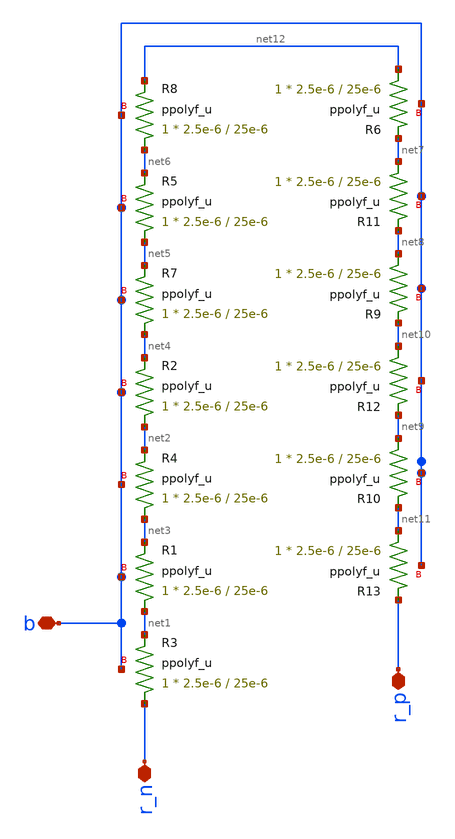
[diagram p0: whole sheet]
** sch_path: designs/libs/core_analog/vref/vref_R2.sch
**.subckt vref_R2 r_p r_n b
*.iopin r_p
*.iopin r_n
*.iopin b
XR1 net1 net3 b ppolyf_u r_width=2.5e-6 r_length=25e-6 m=1
XR2 net2 net4 b ppolyf_u r_width=2.5e-6 r_length=25e-6 m=1
XR3 r_n net1 b ppolyf_u r_width=2.5e-6 r_length=25e-6 m=1
XR4 net3 net2 b ppolyf_u r_width=2.5e-6 r_length=25e-6 m=1
XR5 net5 net6 b ppolyf_u r_width=2.5e-6 r_length=25e-6 m=1
XR7 net4 net5 b ppolyf_u r_width=2.5e-6 r_length=25e-6 m=1
XR8 net6 net12 b ppolyf_u r_width=2.5e-6 r_length=25e-6 m=1
XR6 net12 net7 b ppolyf_u r_width=2.5e-6 r_length=25e-6 m=1
XR9 net8 net10 b ppolyf_u r_width=2.5e-6 r_length=25e-6 m=1
XR10 net9 net11 b ppolyf_u r_width=2.5e-6 r_length=25e-6 m=1
XR11 net7 net8 b ppolyf_u r_width=2.5e-6 r_length=25e-6 m=1
XR12 net10 net9 b ppolyf_u r_width=2.5e-6 r_length=25e-6 m=1
XR13 net11 r_p b ppolyf_u r_width=2.5e-6 r_length=25e-6 m=1
**.ends
.end
